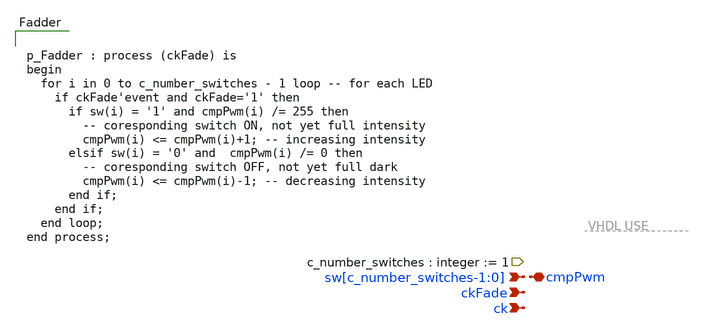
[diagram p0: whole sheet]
** sch_path: xschem/Fadder.sch
**.subckt Fadder ck ckFade sw[c_number_switches-1:0] cmpPwm
*.ipin ck
*.ipin ckFade
*.ipin sw[c_number_switches-1:0]
*.iopin cmpPwm
**** begin user architecture code


p_Fadder : process (ckFade) is
begin
  for i in 0 to c_number_switches - 1 loop -- for each LED
    if ckFade'event and ckFade='1' then
      if sw(i) = '1' and cmpPwm(i) /= 255 then
        -- coresponding switch ON, not yet full intensity
        cmpPwm(i) <= cmpPwm(i)+1; -- increasing intensity
      elsif sw(i) = '0' and  cmpPwm(i) /= 0 then
        -- coresponding switch OFF, not yet full dark
        cmpPwm(i) <= cmpPwm(i)-1; -- decreasing intensity
      end if;
    end if;
  end loop;
end process;


**** end user architecture code
**.ends
.end
